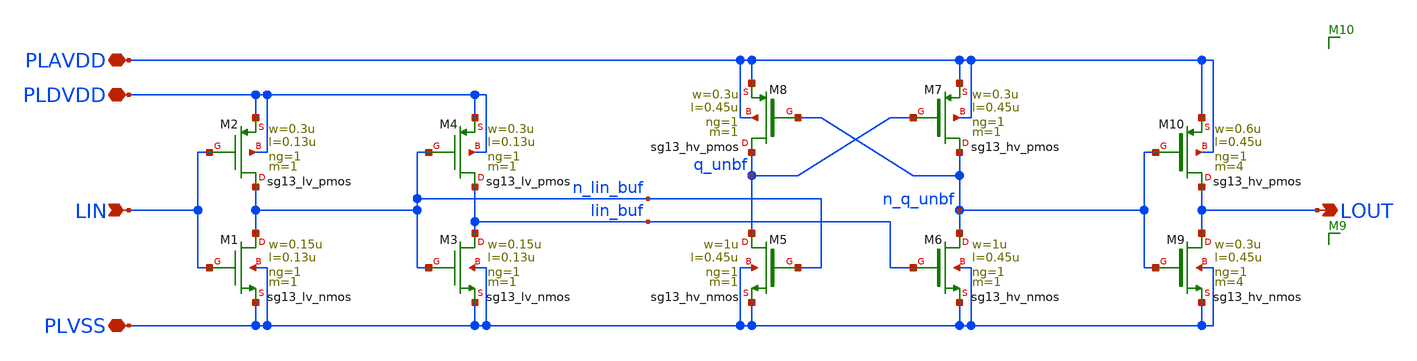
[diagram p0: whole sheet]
** sch_path: xschem/digital_level_translator.sch
**.subckt digital_level_translator PLAVDD PLVSS PLDVDD LIN LOUT
*.iopin PLAVDD
*.iopin PLVSS
*.iopin PLDVDD
*.ipin LIN
*.opin LOUT
XM1 n_lin_buf LIN PLVSS PLVSS sg13_lv_nmos w=0.15u l=0.13u ng=1 m=1 mm_ok=1
XM2 n_lin_buf LIN PLDVDD PLDVDD sg13_lv_pmos w=0.3u l=0.13u ng=1 m=1 mm_ok=1
XM3 lin_buf n_lin_buf PLVSS PLVSS sg13_lv_nmos w=0.15u l=0.13u ng=1 m=1 mm_ok=1
XM4 lin_buf n_lin_buf PLDVDD PLDVDD sg13_lv_pmos w=0.3u l=0.13u ng=1 m=1 mm_ok=1
XM5 q_unbf n_lin_buf PLVSS PLVSS sg13_hv_nmos w=1u l=0.45u ng=1 m=1 mm_ok=1
XM6 n_q_unbf lin_buf PLVSS PLVSS sg13_hv_nmos w=1u l=0.45u ng=1 m=1 mm_ok=1
XM7 n_q_unbf q_unbf PLAVDD PLAVDD sg13_hv_pmos w=0.3u l=0.45u ng=1 m=1 mm_ok=1
XM9 LOUT n_q_unbf PLVSS PLVSS sg13_hv_nmos w=0.3u l=0.45u ng=1 m=4 mm_ok=1
XM10 LOUT n_q_unbf PLAVDD PLAVDD sg13_hv_pmos w=0.6u l=0.45u ng=1 m=4 mm_ok=1
XM8 q_unbf n_q_unbf PLAVDD PLAVDD sg13_hv_pmos w=0.3u l=0.45u ng=1 m=1 mm_ok=1
**.ends
.end
